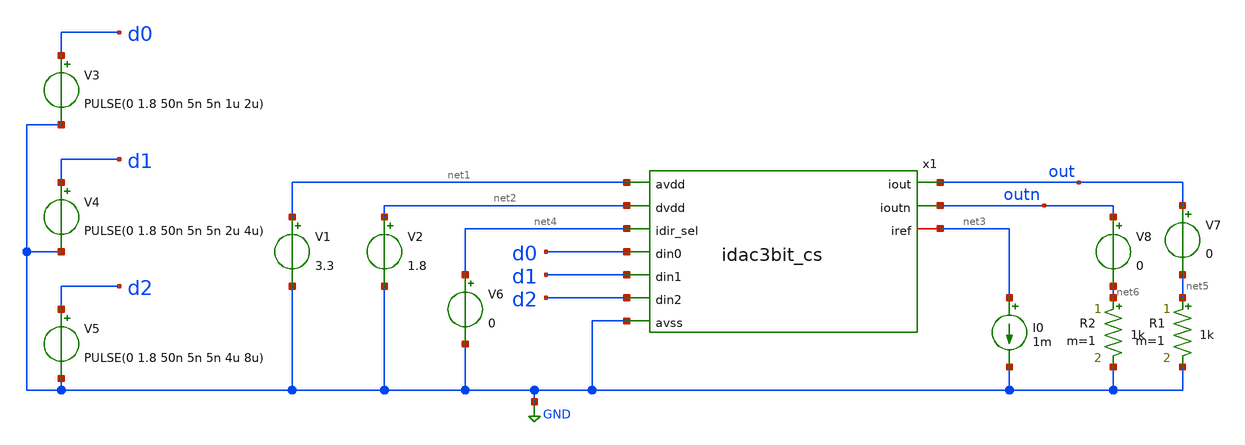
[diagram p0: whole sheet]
** sch_path: xschem/idac3bit_cs_tb.sch
**.subckt idac3bit_cs_tb
V1 net1 GND 3.3
V2 net2 GND 1.8
I0 net3 GND 1m
V3 d0 GND PULSE(0 1.8 50n 5n 5n 1u 2u)
V4 d1 GND PULSE(0 1.8 50n 5n 5n 2u 4u)
V5 d2 GND PULSE(0 1.8 50n 5n 5n 4u 8u)
V6 net4 GND 0
V7 out net5 0
R1 net5 GND 1k m=1
x1 net1 net2 out outn d0 net4 d1 GND d2 net3 idac3bit_cs
V8 outn net6 0
R2 net6 GND 1k m=1
**** begin user architecture code
 .lib $::SKYWATER_MODELS/sky130.lib.spice tt
.include $::SKYWATER_STDCELLS/../../sky130_fd_sc_hvl/spice/sky130_fd_sc_hvl.spice

.param mc_mm_switch=0
.param mc_pr_switch=1



.option wnflag=0
.option savecurrents
.control
save all
tran 1n 20u
plot v(out) v(outn)
write currentmirrortb.raw
op
.endc


**** end user architecture code
**.ends
.GLOBAL GND
.end
